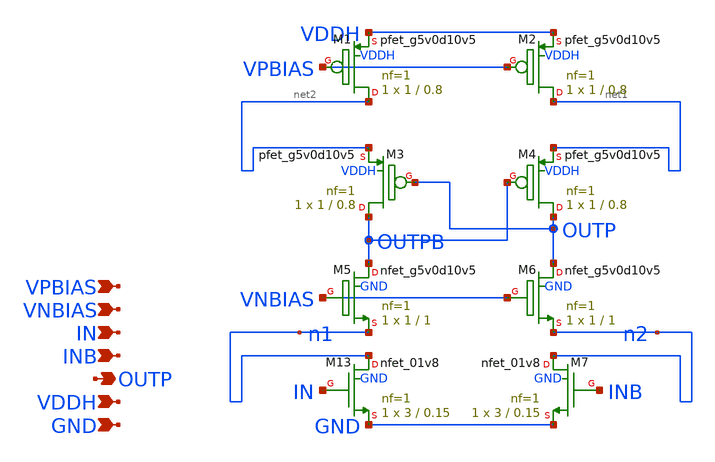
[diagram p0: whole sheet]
** sch_path: xschem/lvsf.sch
**.subckt lvsf IN INB OUTP VDDH GND VPBIAS VNBIAS
*.ipin IN
*.ipin INB
*.opin OUTP
*.ipin VDDH
*.ipin GND
*.ipin VPBIAS
*.ipin VNBIAS
XM13 n1 IN GND GND sky130_fd_pr__nfet_01v8 L=0.15 W=3 nf=1 ad='int((nf+1)/2) * W/nf * 0.29' as='int((nf+2)/2) * W/nf * 0.29'
+ pd='2*int((nf+1)/2) * (W/nf + 0.29)' ps='2*int((nf+2)/2) * (W/nf + 0.29)' nrd='0.29 / W' nrs='0.29 / W'
+ sa=0 sb=0 sd=0 mult=1 m=1
XM1 net2 VPBIAS VDDH VDDH sky130_fd_pr__pfet_g5v0d10v5 L=0.8 W=1 nf=1 ad='int((nf+1)/2) * W/nf * 0.29'
+ as='int((nf+2)/2) * W/nf * 0.29' pd='2*int((nf+1)/2) * (W/nf + 0.29)' ps='2*int((nf+2)/2) * (W/nf + 0.29)'
+ nrd='0.29 / W' nrs='0.29 / W' sa=0 sb=0 sd=0 mult=1 m=1
XM2 net1 VPBIAS VDDH VDDH sky130_fd_pr__pfet_g5v0d10v5 L=0.8 W=1 nf=1 ad='int((nf+1)/2) * W/nf * 0.29'
+ as='int((nf+2)/2) * W/nf * 0.29' pd='2*int((nf+1)/2) * (W/nf + 0.29)' ps='2*int((nf+2)/2) * (W/nf + 0.29)'
+ nrd='0.29 / W' nrs='0.29 / W' sa=0 sb=0 sd=0 mult=1 m=1
XM3 OUTPB OUTP net2 VDDH sky130_fd_pr__pfet_g5v0d10v5 L=0.8 W=1 nf=1 ad='int((nf+1)/2) * W/nf * 0.29'
+ as='int((nf+2)/2) * W/nf * 0.29' pd='2*int((nf+1)/2) * (W/nf + 0.29)' ps='2*int((nf+2)/2) * (W/nf + 0.29)'
+ nrd='0.29 / W' nrs='0.29 / W' sa=0 sb=0 sd=0 mult=1 m=1
XM4 OUTP OUTPB net1 VDDH sky130_fd_pr__pfet_g5v0d10v5 L=0.8 W=1 nf=1 ad='int((nf+1)/2) * W/nf * 0.29'
+ as='int((nf+2)/2) * W/nf * 0.29' pd='2*int((nf+1)/2) * (W/nf + 0.29)' ps='2*int((nf+2)/2) * (W/nf + 0.29)'
+ nrd='0.29 / W' nrs='0.29 / W' sa=0 sb=0 sd=0 mult=1 m=1
XM5 OUTPB VNBIAS n1 GND sky130_fd_pr__nfet_g5v0d10v5 L=1 W=1 nf=1 ad='int((nf+1)/2) * W/nf * 0.29' as='int((nf+2)/2) * W/nf * 0.29'
+ pd='2*int((nf+1)/2) * (W/nf + 0.29)' ps='2*int((nf+2)/2) * (W/nf + 0.29)' nrd='0.29 / W' nrs='0.29 / W'
+ sa=0 sb=0 sd=0 mult=1 m=1
XM6 OUTP VNBIAS n2 GND sky130_fd_pr__nfet_g5v0d10v5 L=1 W=1 nf=1 ad='int((nf+1)/2) * W/nf * 0.29' as='int((nf+2)/2) * W/nf * 0.29'
+ pd='2*int((nf+1)/2) * (W/nf + 0.29)' ps='2*int((nf+2)/2) * (W/nf + 0.29)' nrd='0.29 / W' nrs='0.29 / W'
+ sa=0 sb=0 sd=0 mult=1 m=1
XM7 n2 INB GND GND sky130_fd_pr__nfet_01v8 L=0.15 W=3 nf=1 ad='int((nf+1)/2) * W/nf * 0.29' as='int((nf+2)/2) * W/nf * 0.29'
+ pd='2*int((nf+1)/2) * (W/nf + 0.29)' ps='2*int((nf+2)/2) * (W/nf + 0.29)' nrd='0.29 / W' nrs='0.29 / W'
+ sa=0 sb=0 sd=0 mult=1 m=1
**.ends
.end
